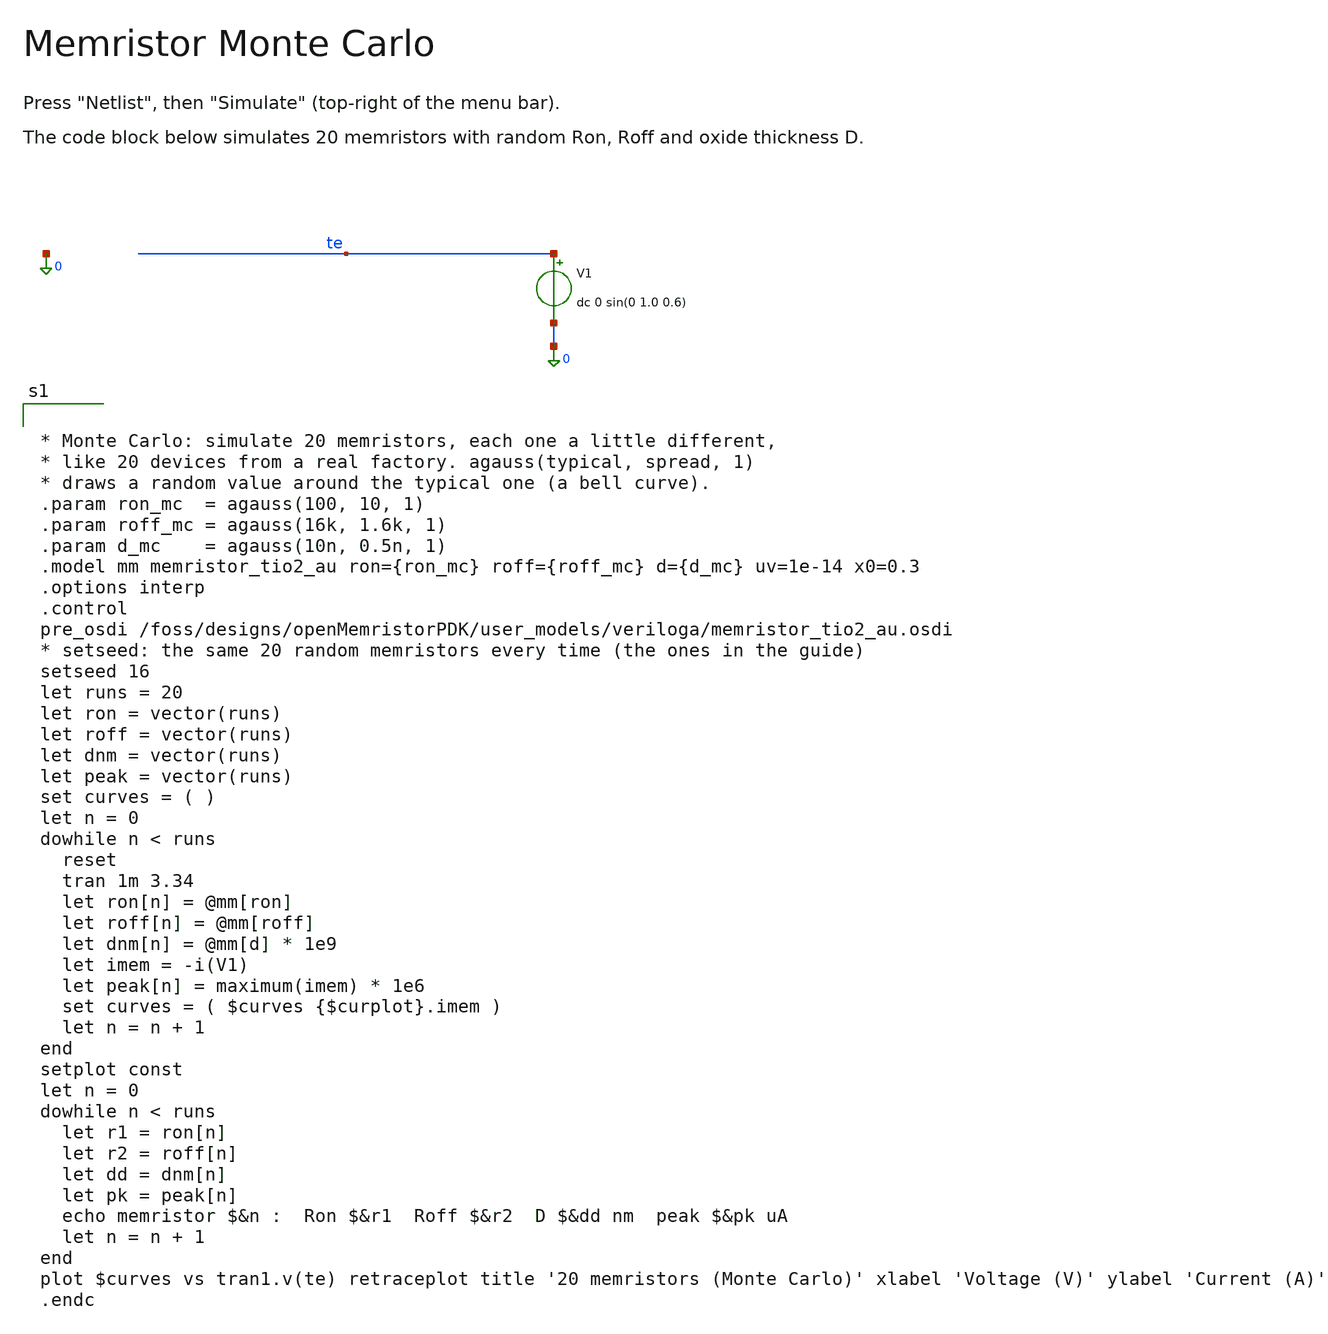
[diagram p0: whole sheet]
** sch_path: libraries/openmemristorpdk_pr/memristor_tio2_au_mc_tb.sch
**.subckt memristor_tio2_au_mc_tb
V1 te 0 dc 0 sin(0 1.0 0.6)
**** begin user architecture code


* Monte Carlo: simulate 20 memristors, each one a little different,
* like 20 devices from a real factory. agauss(typical, spread, 1)
* draws a random value around the typical one (a bell curve).
.param ron_mc  = agauss(100, 10, 1)
.param roff_mc = agauss(16k, 1.6k, 1)
.param d_mc    = agauss(10n, 0.5n, 1)
.model mm memristor_tio2_au ron={ron_mc} roff={roff_mc} d={d_mc} uv=1e-14 x0=0.3
.options interp
.control
pre_osdi /foss/designs/openMemristorPDK/user_models/veriloga/memristor_tio2_au.osdi
* setseed: the same 20 random memristors every time (the ones in the guide)
setseed 16
let runs = 20
let ron = vector(runs)
let roff = vector(runs)
let dnm = vector(runs)
let peak = vector(runs)
set curves = ( )
let n = 0
dowhile n < runs
  reset
  tran 1m 3.34
  let ron[n] = @mm[ron]
  let roff[n] = @mm[roff]
  let dnm[n] = @mm[d] * 1e9
  let imem = -i(V1)
  let peak[n] = maximum(imem) * 1e6
  set curves = ( $curves {$curplot}.imem )
  let n = n + 1
end
setplot const
let n = 0
dowhile n < runs
  let r1 = ron[n]
  let r2 = roff[n]
  let dd = dnm[n]
  let pk = peak[n]
  echo memristor $&n :  Ron $&r1  Roff $&r2  D $&dd nm  peak $&pk uA
  let n = n + 1
end
plot $curves vs tran1.v(te) retraceplot title '20 memristors (Monte Carlo)' xlabel 'Voltage (V)' ylabel
+ 'Current (A)'
.endc


**** end user architecture code
**.ends
.end
